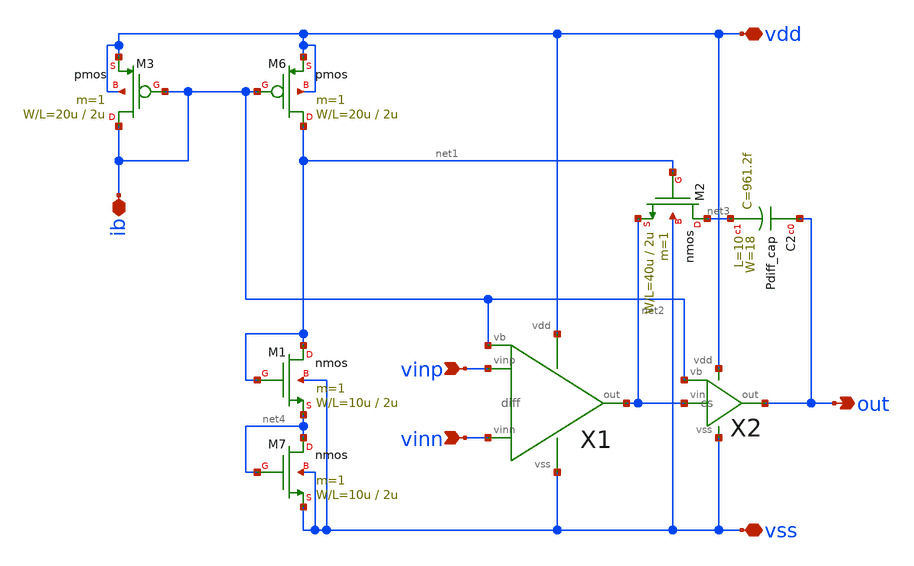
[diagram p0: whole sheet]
** sch_path: OR1/PTC06/opamp/opamp.sch
**.subckt opamp vinp vinn out vdd vss ib
*.ipin vinp
*.ipin vinn
*.opin out
*.iopin vdd
*.iopin vss
*.iopin ib
X1 vinp vinn net2 vdd vss ib diff
X2 net2 ib out vdd vss cs
M3 ib ib vdd vdd pmos L=2u W=20u m=1
M2 net3 net1 net2 vss nmos L=2u W=40u m=1
M6 net1 ib vdd vdd pmos L=2u W=20u m=1
M1 net1 net1 net4 vss nmos L=2u W=10u m=1
M7 net4 net4 vss vss nmos L=2u W=10u m=1
C2 out net3 Pdiff_cap W=18 L=10
**.ends

* expanding   symbol:  diff.sym # of pins=6
** sym_path: diff.sym
** sch_path: diff.sch
.subckt diff vinp vinn out vdd vss vb
*.ipin vinn
*.ipin vinp
*.ipin vb
*.opin out
*.iopin vdd
*.iopin vss
M5 net2 vb vdd vdd pmos L=2u W=40u m=1
M1 net1 vinn net2 net2 pmos L=2u W=200u m=1
M2 out vinp net2 net2 pmos L=2u W=200u m=1
M3 net1 net1 vss vss nmos L=2u W=10u m=1
M4 out net1 vss vss nmos L=2u W=10u m=1
.ends


* expanding   symbol:  cs.sym # of pins=5
** sym_path: cs.sym
** sch_path: cs.sch
.subckt cs vin vb out vdd vss
*.ipin vb
*.ipin vin
*.opin out
*.iopin vss
*.iopin vdd
M6 out vb vdd vdd pmos L=2u W=400u m=1
M7 out vin vss vss nmos L=2u W=200u m=1
.ends

.end
